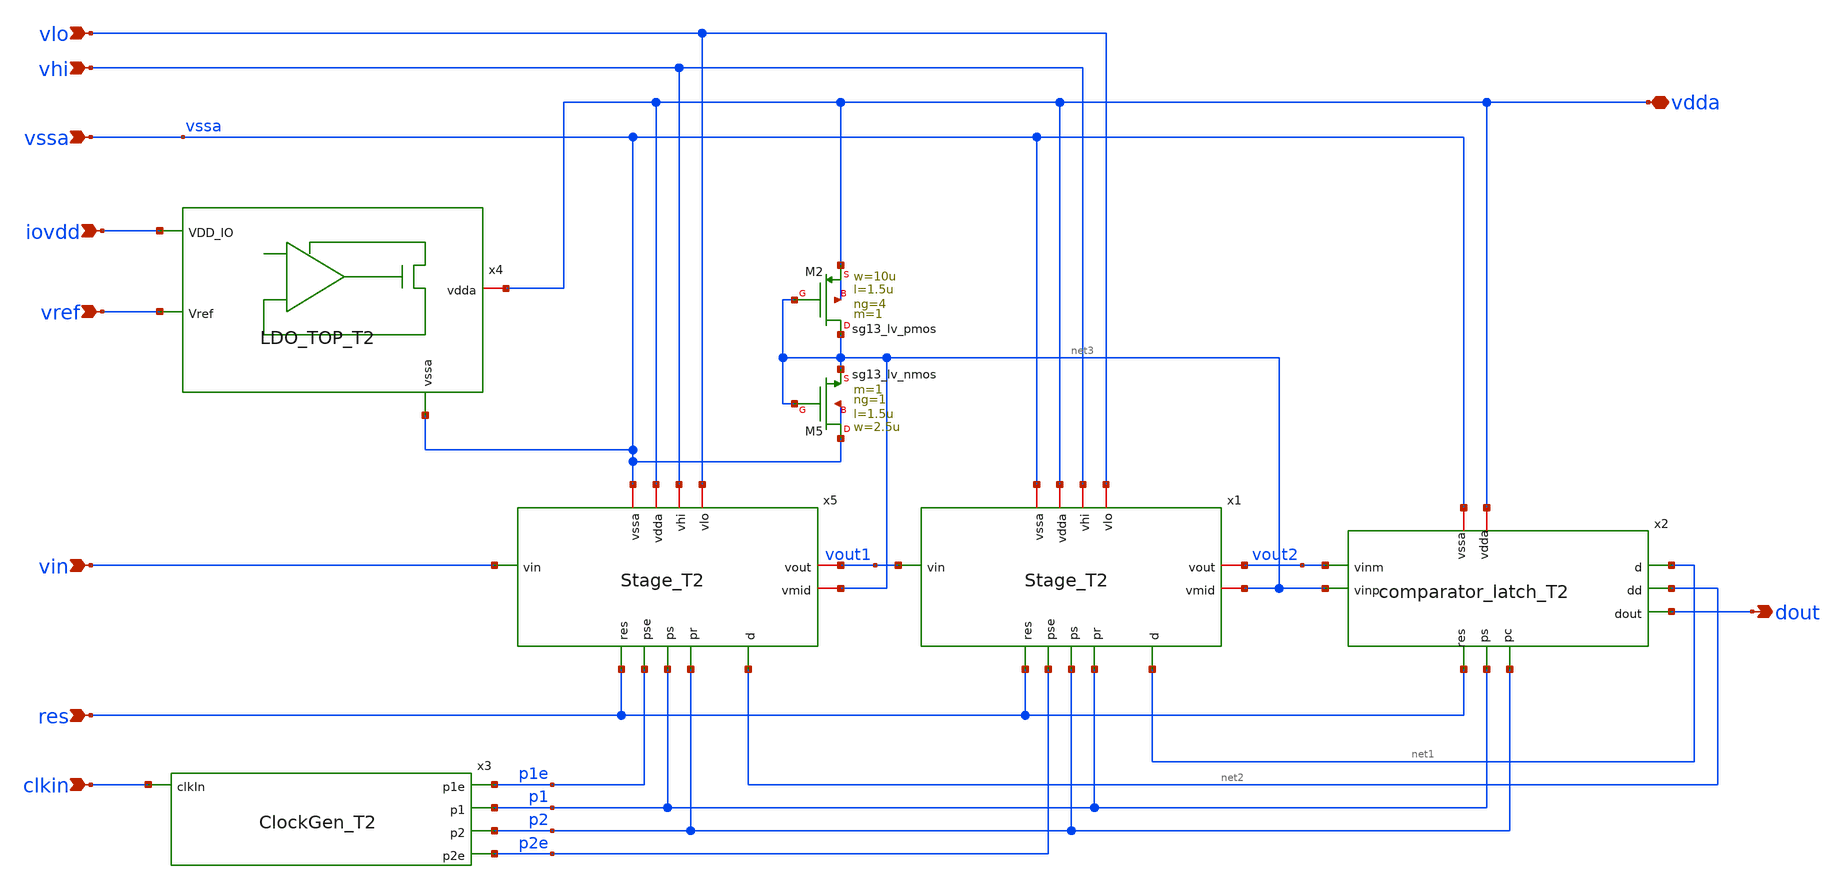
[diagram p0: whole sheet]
** sch_path: 5_Design/4_Layout/Team 2 - Transformer Monster Tractors/xschem/Team_2.sch
**.subckt Team_2 clkin res dout vlo vssa vhi vin iovdd vref vdda
*.ipin clkin
*.ipin res
*.opin dout
*.ipin vlo
*.ipin vssa
*.ipin vhi
*.ipin vin
*.ipin iovdd
*.ipin vref
*.iopin vdda
XM2 net3 net3 vdda vdda sg13_lv_pmos w=10u l=1.5u ng=4 m=1 mm_ok=1
XM5 vssa net3 net3 vssa sg13_lv_nmos w=2.5u l=1.5u ng=1 m=1 mm_ok=1
x5 net3 res p1e p1 p2 vhi vdda vin vssa net2 vlo vout1 Stage_T2
x2 vdda p2 net1 net2 dout net3 res vssa p1 vout2 comparator_latch_T2
x3 p1e clkin p1 p2 p2e ClockGen_T2
x1 net3 res p2e p2 p1 vhi vdda vout1 vssa net1 vlo vout2 Stage_T2
x4 iovdd vref vdda vssa LDO_TOP_T2
**.ends
.end
